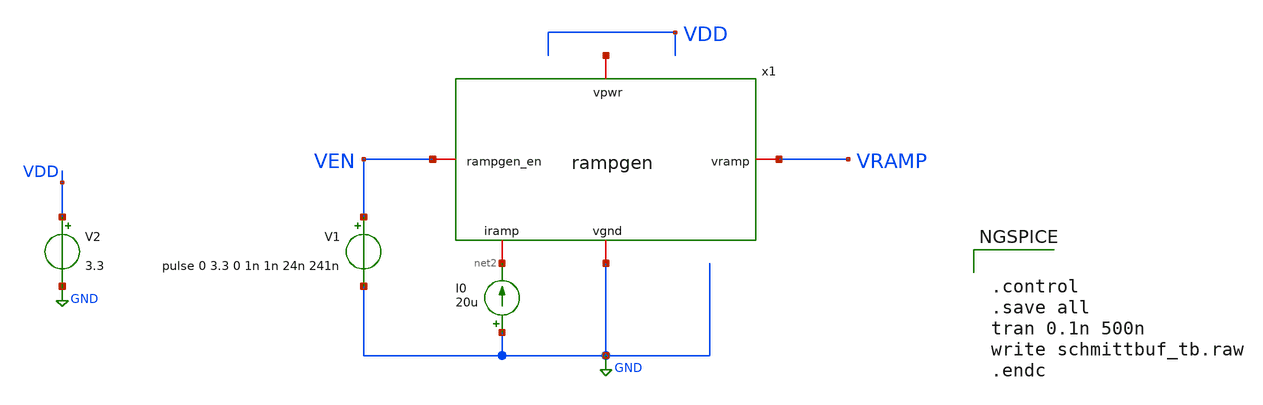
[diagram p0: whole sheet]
** sch_path: images/iic-osic-tools/addons/examples/open-pmic/design/oscillator/rampgen_tb.sch
**.subckt rampgen_tb
x1 net1 GND net2 VRAMP VEN rampgen
I0 GND net2 20u
V1 VEN GND pulse 0 3.3 0 1n 1n 24n 241n
V2 VDD GND 3.3
**** begin user architecture code

.include $::SKYWATER_MODELS/cells/nfet_01v8/sky130_fd_pr__nfet_01v8__tt.corner.spice
.include $::SKYWATER_MODELS/cells/nfet_01v8_lvt/sky130_fd_pr__nfet_01v8_lvt__tt.corner.spice
.include $::SKYWATER_MODELS/cells/pfet_01v8/sky130_fd_pr__pfet_01v8__tt.corner.spice
.include $::SKYWATER_MODELS/cells/nfet_03v3_nvt/sky130_fd_pr__nfet_03v3_nvt__tt.corner.spice
.include $::SKYWATER_MODELS/cells/nfet_05v0_nvt/sky130_fd_pr__nfet_05v0_nvt__tt.corner.spice
.include $::SKYWATER_MODELS/cells/esd_nfet_01v8/sky130_fd_pr__esd_nfet_01v8__tt.corner.spice
.include $::SKYWATER_MODELS/cells/pfet_01v8_lvt/sky130_fd_pr__pfet_01v8_lvt__tt.corner.spice
.include $::SKYWATER_MODELS/cells/pfet_01v8_hvt/sky130_fd_pr__pfet_01v8_hvt__tt.corner.spice
.include $::SKYWATER_MODELS/cells/esd_pfet_g5v0d10v5/sky130_fd_pr__esd_pfet_g5v0d10v5__tt.corner.spice
.include $::SKYWATER_MODELS/cells/pfet_g5v0d10v5/sky130_fd_pr__pfet_g5v0d10v5__tt.corner.spice
.include $::SKYWATER_MODELS/cells/pfet_g5v0d16v0/sky130_fd_pr__pfet_g5v0d16v0__tt.corner.spice
.include $::SKYWATER_MODELS/cells/nfet_g5v0d10v5/sky130_fd_pr__nfet_g5v0d10v5__tt.corner.spice
.include $::SKYWATER_MODELS/cells/nfet_g5v0d16v0/sky130_fd_pr__nfet_g5v0d16v0__tt_discrete.corner.spice
.include $::SKYWATER_MODELS/cells/esd_nfet_g5v0d10v5/sky130_fd_pr__esd_nfet_g5v0d10v5__tt.corner.spice
.include $::SKYWATER_MODELS/models/corners/tt/nonfet.spice
* Mismatch parameters
.include $::SKYWATER_MODELS/cells/nfet_01v8/sky130_fd_pr__nfet_01v8__mismatch.corner.spice
.include $::SKYWATER_MODELS/cells/pfet_01v8/sky130_fd_pr__pfet_01v8__mismatch.corner.spice
.include $::SKYWATER_MODELS/cells/nfet_01v8_lvt/sky130_fd_pr__nfet_01v8_lvt__mismatch.corner.spice
.include $::SKYWATER_MODELS/cells/pfet_01v8_lvt/sky130_fd_pr__pfet_01v8_lvt__mismatch.corner.spice
.include $::SKYWATER_MODELS/cells/pfet_01v8_hvt/sky130_fd_pr__pfet_01v8_hvt__mismatch.corner.spice
.include $::SKYWATER_MODELS/cells/nfet_g5v0d10v5/sky130_fd_pr__nfet_g5v0d10v5__mismatch.corner.spice
.include $::SKYWATER_MODELS/cells/pfet_g5v0d10v5/sky130_fd_pr__pfet_g5v0d10v5__mismatch.corner.spice
.include $::SKYWATER_MODELS/cells/nfet_05v0_nvt/sky130_fd_pr__nfet_05v0_nvt__mismatch.corner.spice
.include $::SKYWATER_MODELS/cells/nfet_03v3_nvt/sky130_fd_pr__nfet_03v3_nvt__mismatch.corner.spice
* Resistor$::SKYWATER_MODELS/Capacitor
.include $::SKYWATER_MODELS/models/r+c/res_typical__cap_typical.spice
.include $::SKYWATER_MODELS/models/r+c/res_typical__cap_typical__lin.spice
* Special cells
.include $::SKYWATER_MODELS/models/corners/tt/specialized_cells.spice
* All models
.include $::SKYWATER_MODELS/models/all.spice
* Corner
.include $::SKYWATER_MODELS/models/corners/tt/rf.spice



.control
.save all
tran 0.1n 500n
write schmittbuf_tb.raw
.endc


**** end user architecture code
**.ends
.GLOBAL GND
**** begin user architecture code
[sky130_models]
**** end user architecture code
.end
